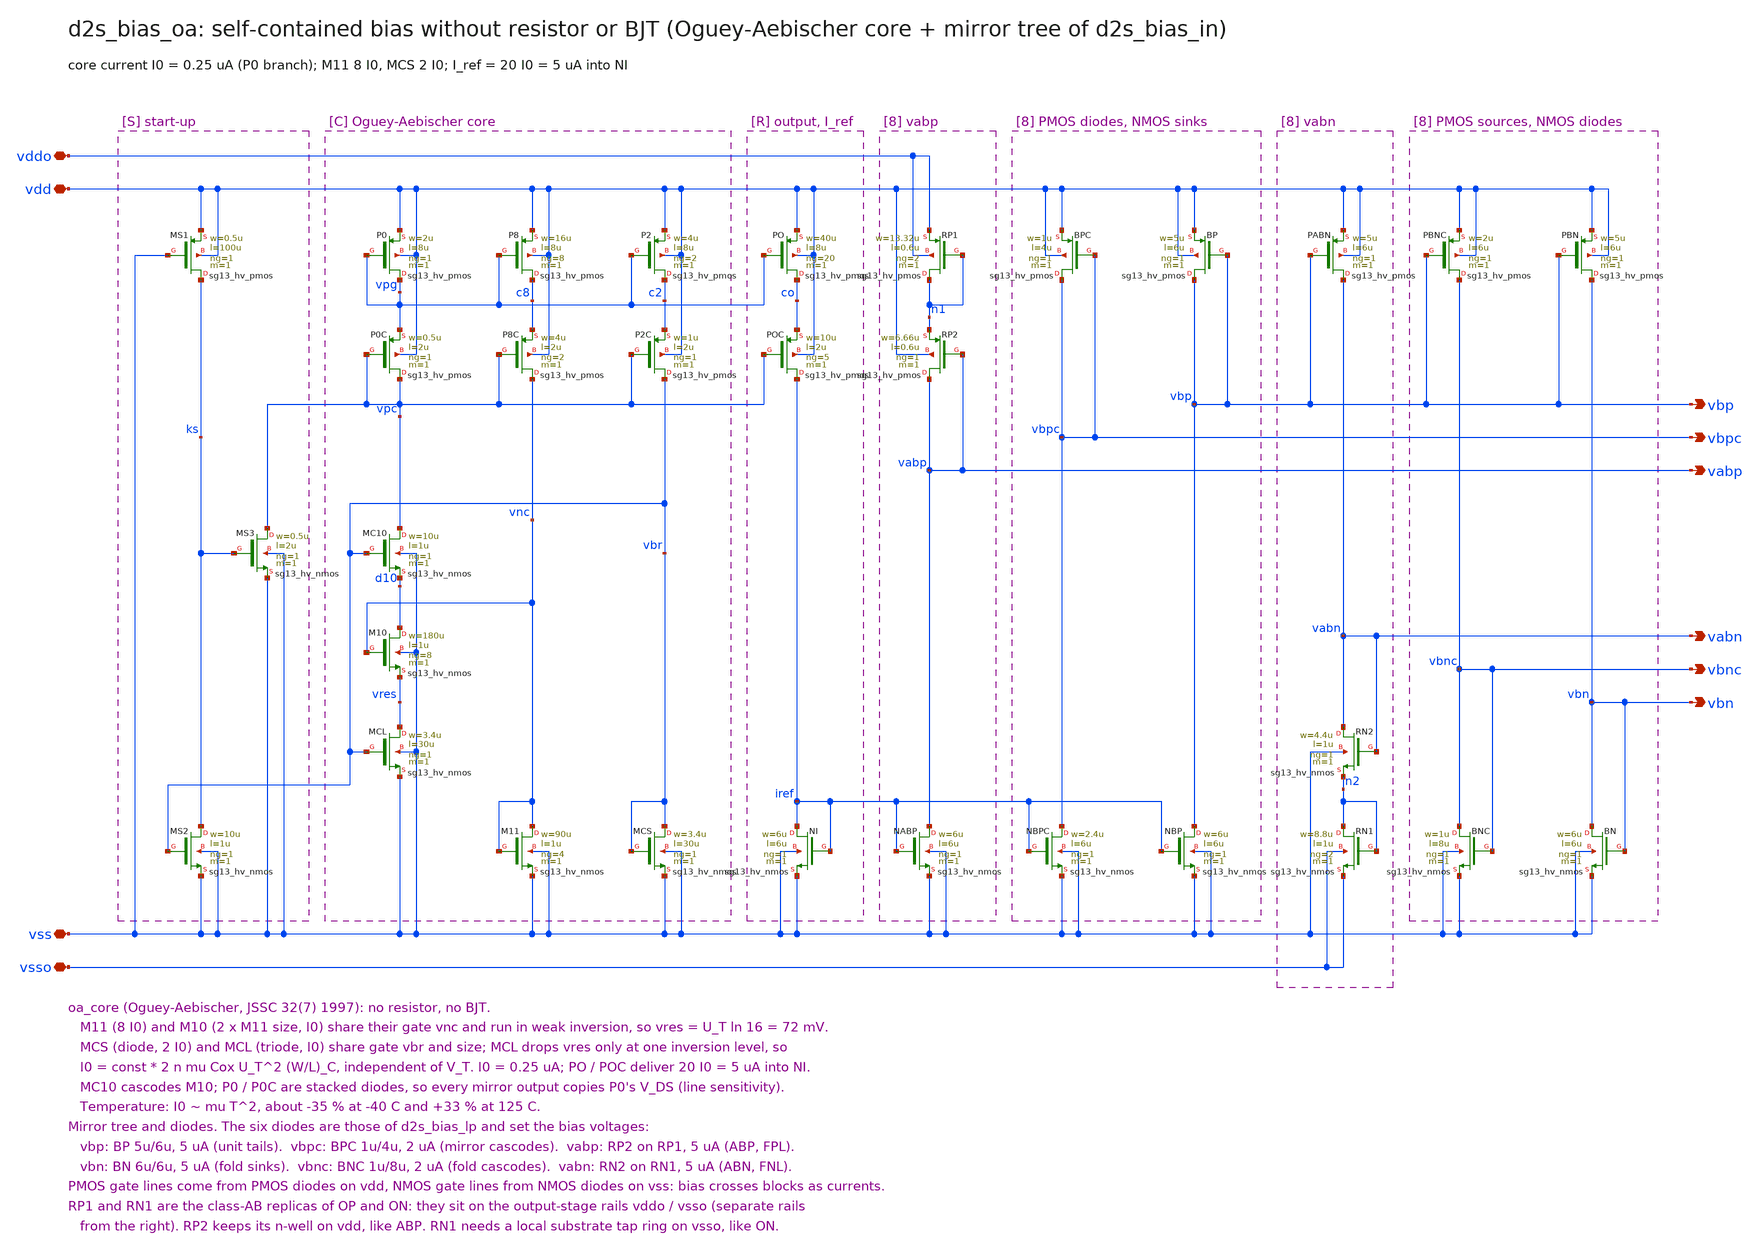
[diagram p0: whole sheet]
** sch_path: sudelbuecher/design_considerations/class_ab_pad_driver/improvements/xschem/d2s_bias_oa.sch
**.subckt d2s_bias_oa vdd vss vddo vsso vbp vbn vbpc vbnc vabp vabn
*.iopin vdd
*.iopin vss
*.iopin vddo
*.iopin vsso
*.opin vbp
*.opin vbn
*.opin vbpc
*.opin vbnc
*.opin vabp
*.opin vabn
XMS1 ks vss vdd vdd sg13_hv_pmos w=0.5u l=100u ng=1 m=1 mm_ok=1
XMS2 ks vbr vss vss sg13_hv_nmos w=10u l=1u ng=1 m=1 mm_ok=1
XMS3 vpc ks vss vss sg13_hv_nmos w=0.5u l=2u ng=1 m=1 mm_ok=1
XP0 vpg vpg vdd vdd sg13_hv_pmos w=2u l=8u ng=1 m=1 mm_ok=1
XP0C vpc vpc vpg vdd sg13_hv_pmos w=0.5u l=2u ng=1 m=1 mm_ok=1
XMC10 vpc vbr d10 vss sg13_hv_nmos w=10u l=1u ng=1 m=1 mm_ok=1
XM10 d10 vnc vres vss sg13_hv_nmos w=180u l=1u ng=8 m=1 mm_ok=1
XMCL vres vbr vss vss sg13_hv_nmos w=3.4u l=30u ng=1 m=1 mm_ok=1
XP8 c8 vpg vdd vdd sg13_hv_pmos w=16u l=8u ng=8 m=1 mm_ok=1
XP8C vnc vpc c8 vdd sg13_hv_pmos w=4u l=2u ng=2 m=1 mm_ok=1
XM11 vnc vnc vss vss sg13_hv_nmos w=90u l=1u ng=4 m=1 mm_ok=1
XP2 c2 vpg vdd vdd sg13_hv_pmos w=4u l=8u ng=2 m=1 mm_ok=1
XP2C vbr vpc c2 vdd sg13_hv_pmos w=1u l=2u ng=1 m=1 mm_ok=1
XMCS vbr vbr vss vss sg13_hv_nmos w=3.4u l=30u ng=1 m=1 mm_ok=1
XPO co vpg vdd vdd sg13_hv_pmos w=40u l=8u ng=20 m=1 mm_ok=1
XPOC iref vpc co vdd sg13_hv_pmos w=10u l=2u ng=5 m=1 mm_ok=1
XNI iref iref vss vss sg13_hv_nmos w=6u l=6u ng=1 m=1 mm_ok=1
XBPC vbpc vbpc vdd vdd sg13_hv_pmos w=1u l=4u ng=1 m=1 mm_ok=1
XNBPC vbpc iref vss vss sg13_hv_nmos w=2.4u l=6u ng=1 m=1 mm_ok=1
XBP vbp vbp vdd vdd sg13_hv_pmos w=5u l=6u ng=1 m=1 mm_ok=1
XNBP vbp iref vss vss sg13_hv_nmos w=6u l=6u ng=1 m=1 mm_ok=1
XRP1 n1 n1 vddo vddo sg13_hv_pmos w=13.32u l=0.6u ng=2 m=1 mm_ok=1
XRP2 vabp vabp n1 vdd sg13_hv_pmos w=6.66u l=0.6u ng=1 m=1 mm_ok=1
XNABP vabp iref vss vss sg13_hv_nmos w=6u l=6u ng=1 m=1 mm_ok=1
XPBNC vbnc vbp vdd vdd sg13_hv_pmos w=2u l=6u ng=1 m=1 mm_ok=1
XBNC vbnc vbnc vss vss sg13_hv_nmos w=1u l=8u ng=1 m=1 mm_ok=1
XPBN vbn vbp vdd vdd sg13_hv_pmos w=5u l=6u ng=1 m=1 mm_ok=1
XBN vbn vbn vss vss sg13_hv_nmos w=6u l=6u ng=1 m=1 mm_ok=1
XPABN vabn vbp vdd vdd sg13_hv_pmos w=5u l=6u ng=1 m=1 mm_ok=1
XRN2 vabn vabn n2 vss sg13_hv_nmos w=4.4u l=1u ng=1 m=1 mm_ok=1
XRN1 n2 n2 vsso vsso sg13_hv_nmos w=8.8u l=1u ng=2 m=1 mm_ok=1
**.ends
.end
